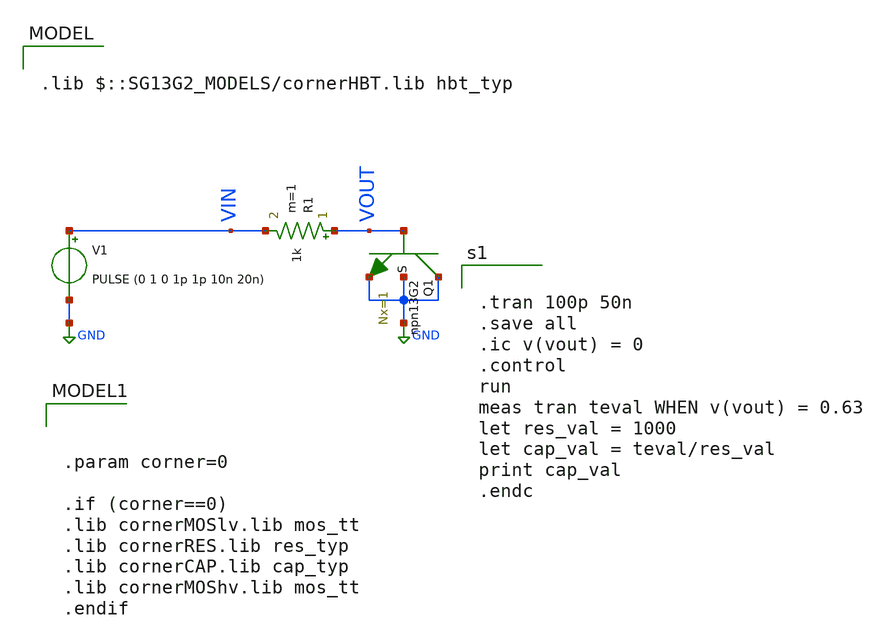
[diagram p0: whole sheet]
** sch_path: DelayLine/others/single mos/tb_cgate-ext_circuit.sch
**.subckt tb_cgate-ext_circuit
R1 VOUT VIN 1k m=1
V1 VIN GND PULSE (0 1 0 1p 1p 10n 20n)
XQ1 GND VOUT GND GND npn13G2 Nx=1 mm_ok=1
**** begin user architecture code


.tran 100p 50n
.save all
.ic v(vout) = 0
.control
run
meas tran teval WHEN v(vout) = 0.63
let res_val = 1000
let cap_val = teval/res_val
print cap_val
.endc




.param corner=0

.if (corner==0)
.lib cornerMOSlv.lib mos_tt
.lib cornerRES.lib res_typ
.lib cornerCAP.lib cap_typ
.lib cornerMOShv.lib mos_tt
.endif


.lib $::SG13G2_MODELS/cornerHBT.lib hbt_typ

**** end user architecture code
**.ends
.GLOBAL GND
.end
